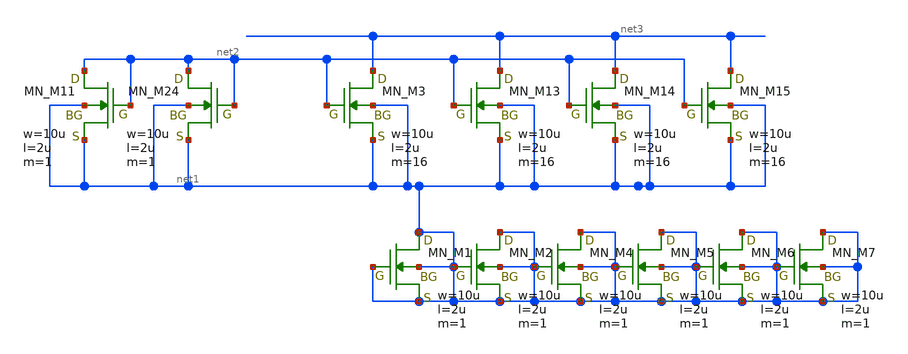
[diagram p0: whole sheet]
** sch_path: member_project/JJY_Receiver/Masahiro/jjy_recv/OBUF_SSF/NMOS640um_CM.sch
**.subckt NMOS640um_CM
XM3 net3 net2 net1 net1 NMOS w=10u l=2u as=0 ad=0 ps=0 pd=0 nrd=0 nrs=0 m=16
XM11 net2 net2 net1 net1 NMOS w=10u l=2u as=0 ad=0 ps=0 pd=0 nrd=0 nrs=0 m=1
XM13 net3 net2 net1 net1 NMOS w=10u l=2u as=0 ad=0 ps=0 pd=0 nrd=0 nrs=0 m=16
XM14 net3 net2 net1 net1 NMOS w=10u l=2u as=0 ad=0 ps=0 pd=0 nrd=0 nrs=0 m=16
XM15 net3 net2 net1 net1 NMOS w=10u l=2u as=0 ad=0 ps=0 pd=0 nrd=0 nrs=0 m=16
XM24 net2 net2 net1 net1 NMOS w=10u l=2u as=0 ad=0 ps=0 pd=0 nrd=0 nrs=0 m=1
XM1 net1 net1 net1 net1 NMOS w=10u l=2u as=0 ad=0 ps=0 pd=0 nrd=0 nrs=0 m=1
XM2 net1 net1 net1 net1 NMOS w=10u l=2u as=0 ad=0 ps=0 pd=0 nrd=0 nrs=0 m=1
XM4 net1 net1 net1 net1 NMOS w=10u l=2u as=0 ad=0 ps=0 pd=0 nrd=0 nrs=0 m=1
XM5 net1 net1 net1 net1 NMOS w=10u l=2u as=0 ad=0 ps=0 pd=0 nrd=0 nrs=0 m=1
XM6 net1 net1 net1 net1 NMOS w=10u l=2u as=0 ad=0 ps=0 pd=0 nrd=0 nrs=0 m=1
XM7 net1 net1 net1 net1 NMOS w=10u l=2u as=0 ad=0 ps=0 pd=0 nrd=0 nrs=0 m=1
**.ends
.end
